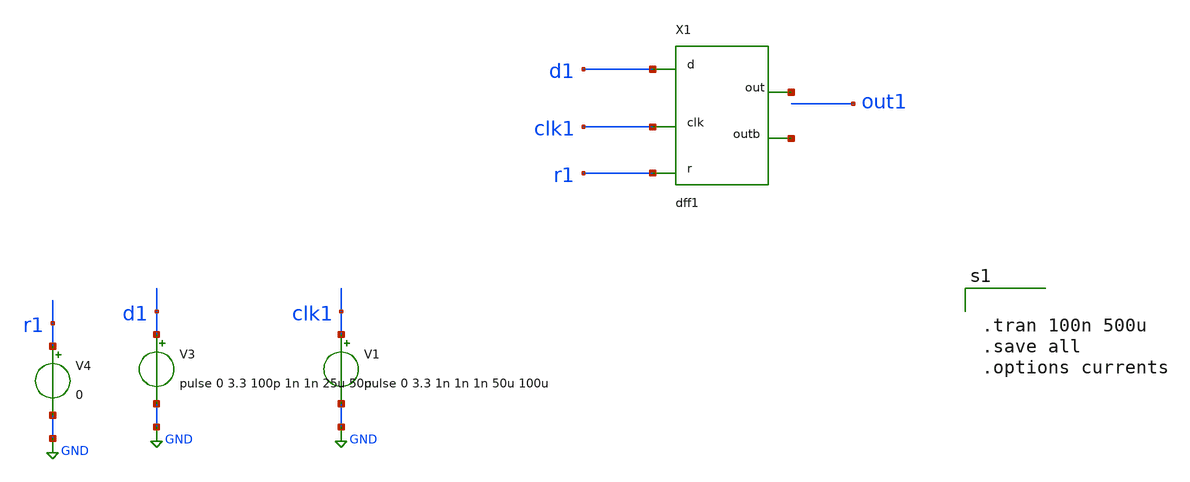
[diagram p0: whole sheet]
** sch_path: xschem/FDC/dff_sym_check.sch
**.subckt dff_sym_check
V1 clk1 GND pulse 0 3.3 1n 1n 1n 50u 100u
V3 d1 GND pulse 0 3.3 100p 1n 1n 25u 50u
V4 r1 GND 0
X1 clk1 d1 r1 net1 net2 dff1
**** begin user architecture code
  .lib /home/vinodhini/open_pdks/sky130/sky130A/libs.tech/ngspice/sky130.lib.spice tt


.tran 100n 500u
.save all
.options currents

**** end user architecture code
**.ends

* expanding   symbol:  /home/vinodhini/Documents/dff1.sym # of pins=5
** sym_path: xschem/FDC/dff1.sym
** sch_path: xschem/FDC/dff1.sch
.subckt dff1 clk d r q qbar
*.ipin clk
*.ipin d
*.ipin r
*.opin q
*.opin qbar
XM1 net2 clkbar net1 net1 sky130_fd_pr__nfet_g5v0d10v5 L=0.5 W=1 nf=1 ad='int((nf+1)/2) * W/nf * 0.29'
+ as='int((nf+2)/2) * W/nf * 0.29' pd='2*int((nf+1)/2) * (W/nf + 0.29)' ps='2*int((nf+2)/2) * (W/nf + 0.29)'
+ nrd='0.29 / W' nrs='0.29 / W' sa=0 sb=0 sd=0 mult=1 m=1
XM2 net2 dbar vdd vdd sky130_fd_pr__pfet_g5v0d10v5 L=0.5 W=2 nf=1 ad='int((nf+1)/2) * W/nf * 0.29' as='int((nf+2)/2) * W/nf * 0.29'
+ pd='2*int((nf+1)/2) * (W/nf + 0.29)' ps='2*int((nf+2)/2) * (W/nf + 0.29)' nrd='0.29 / W' nrs='0.29 / W'
+ sa=0 sb=0 sd=0 mult=1 m=1
XM3 out2 net2 vdd vdd sky130_fd_pr__pfet_g5v0d10v5 L=0.5 W=2 nf=1 ad='int((nf+1)/2) * W/nf * 0.29' as='int((nf+2)/2) * W/nf * 0.29'
+ pd='2*int((nf+1)/2) * (W/nf + 0.29)' ps='2*int((nf+2)/2) * (W/nf + 0.29)' nrd='0.29 / W' nrs='0.29 / W'
+ sa=0 sb=0 sd=0 mult=1 m=1
XM4 net1 dbar GND GND sky130_fd_pr__nfet_g5v0d10v5 L=0.5 W=1 nf=1 ad='int((nf+1)/2) * W/nf * 0.29' as='int((nf+2)/2) * W/nf * 0.29'
+ pd='2*int((nf+1)/2) * (W/nf + 0.29)' ps='2*int((nf+2)/2) * (W/nf + 0.29)' nrd='0.29 / W' nrs='0.29 / W'
+ sa=0 sb=0 sd=0 mult=1 m=1
XM5 out2 net2 GND GND sky130_fd_pr__nfet_g5v0d10v5 L=0.5 W=1 nf=1 ad='int((nf+1)/2) * W/nf * 0.29' as='int((nf+2)/2) * W/nf * 0.29'
+ pd='2*int((nf+1)/2) * (W/nf + 0.29)' ps='2*int((nf+2)/2) * (W/nf + 0.29)' nrd='0.29 / W' nrs='0.29 / W'
+ sa=0 sb=0 sd=0 mult=1 m=1
XM6 net2 clkbar vdd vdd sky130_fd_pr__pfet_g5v0d10v5 L=0.5 W=2 nf=1 ad='int((nf+1)/2) * W/nf * 0.29'
+ as='int((nf+2)/2) * W/nf * 0.29' pd='2*int((nf+1)/2) * (W/nf + 0.29)' ps='2*int((nf+2)/2) * (W/nf + 0.29)'
+ nrd='0.29 / W' nrs='0.29 / W' sa=0 sb=0 sd=0 mult=1 m=1
XM7 net4 d net3 net3 sky130_fd_pr__nfet_g5v0d10v5 L=0.5 W=1 nf=1 ad='int((nf+1)/2) * W/nf * 0.29' as='int((nf+2)/2) * W/nf * 0.29'
+ pd='2*int((nf+1)/2) * (W/nf + 0.29)' ps='2*int((nf+2)/2) * (W/nf + 0.29)' nrd='0.29 / W' nrs='0.29 / W'
+ sa=0 sb=0 sd=0 mult=1 m=1
XM8 net4 clkbar vdd vdd sky130_fd_pr__pfet_g5v0d10v5 L=0.5 W=2 nf=1 ad='int((nf+1)/2) * W/nf * 0.29'
+ as='int((nf+2)/2) * W/nf * 0.29' pd='2*int((nf+1)/2) * (W/nf + 0.29)' ps='2*int((nf+2)/2) * (W/nf + 0.29)'
+ nrd='0.29 / W' nrs='0.29 / W' sa=0 sb=0 sd=0 mult=1 m=1
XM9 out1 net4 vdd vdd sky130_fd_pr__pfet_g5v0d10v5 L=0.5 W=2 nf=1 ad='int((nf+1)/2) * W/nf * 0.29' as='int((nf+2)/2) * W/nf * 0.29'
+ pd='2*int((nf+1)/2) * (W/nf + 0.29)' ps='2*int((nf+2)/2) * (W/nf + 0.29)' nrd='0.29 / W' nrs='0.29 / W'
+ sa=0 sb=0 sd=0 mult=1 m=1
XM10 net3 clkbar GND GND sky130_fd_pr__nfet_g5v0d10v5 L=0.5 W=1 nf=1 ad='int((nf+1)/2) * W/nf * 0.29'
+ as='int((nf+2)/2) * W/nf * 0.29' pd='2*int((nf+1)/2) * (W/nf + 0.29)' ps='2*int((nf+2)/2) * (W/nf + 0.29)'
+ nrd='0.29 / W' nrs='0.29 / W' sa=0 sb=0 sd=0 mult=1 m=1
XM11 out1 net4 GND GND sky130_fd_pr__nfet_g5v0d10v5 L=0.5 W=1 nf=1 ad='int((nf+1)/2) * W/nf * 0.29' as='int((nf+2)/2) * W/nf * 0.29'
+ pd='2*int((nf+1)/2) * (W/nf + 0.29)' ps='2*int((nf+2)/2) * (W/nf + 0.29)' nrd='0.29 / W' nrs='0.29 / W'
+ sa=0 sb=0 sd=0 mult=1 m=1
XM12 net4 d vdd vdd sky130_fd_pr__pfet_g5v0d10v5 L=0.5 W=2 nf=1 ad='int((nf+1)/2) * W/nf * 0.29' as='int((nf+2)/2) * W/nf * 0.29'
+ pd='2*int((nf+1)/2) * (W/nf + 0.29)' ps='2*int((nf+2)/2) * (W/nf + 0.29)' nrd='0.29 / W' nrs='0.29 / W'
+ sa=0 sb=0 sd=0 mult=1 m=1
XM13 out3 out1 GND GND sky130_fd_pr__nfet_g5v0d10v5 L=0.5 W=1 nf=1 ad='int((nf+1)/2) * W/nf * 0.29' as='int((nf+2)/2) * W/nf * 0.29'
+ pd='2*int((nf+1)/2) * (W/nf + 0.29)' ps='2*int((nf+2)/2) * (W/nf + 0.29)' nrd='0.29 / W' nrs='0.29 / W'
+ sa=0 sb=0 sd=0 mult=1 m=1
XM15 out3 out4 GND GND sky130_fd_pr__nfet_g5v0d10v5 L=0.5 W=1 nf=1 ad='int((nf+1)/2) * W/nf * 0.29' as='int((nf+2)/2) * W/nf * 0.29'
+ pd='2*int((nf+1)/2) * (W/nf + 0.29)' ps='2*int((nf+2)/2) * (W/nf + 0.29)' nrd='0.29 / W' nrs='0.29 / W'
+ sa=0 sb=0 sd=0 mult=1 m=1
XM16 net5 out1 vdd vdd sky130_fd_pr__pfet_g5v0d10v5 L=0.5 W=2 nf=1 ad='int((nf+1)/2) * W/nf * 0.29' as='int((nf+2)/2) * W/nf * 0.29'
+ pd='2*int((nf+1)/2) * (W/nf + 0.29)' ps='2*int((nf+2)/2) * (W/nf + 0.29)' nrd='0.29 / W' nrs='0.29 / W'
+ sa=0 sb=0 sd=0 mult=1 m=1
XM14 out3 out4 net5 net5 sky130_fd_pr__pfet_g5v0d10v5 L=0.5 W=2 nf=1 ad='int((nf+1)/2) * W/nf * 0.29'
+ as='int((nf+2)/2) * W/nf * 0.29' pd='2*int((nf+1)/2) * (W/nf + 0.29)' ps='2*int((nf+2)/2) * (W/nf + 0.29)'
+ nrd='0.29 / W' nrs='0.29 / W' sa=0 sb=0 sd=0 mult=1 m=1
XM17 out4 out3 GND GND sky130_fd_pr__nfet_g5v0d10v5 L=0.5 W=1 nf=1 ad='int((nf+1)/2) * W/nf * 0.29' as='int((nf+2)/2) * W/nf * 0.29'
+ pd='2*int((nf+1)/2) * (W/nf + 0.29)' ps='2*int((nf+2)/2) * (W/nf + 0.29)' nrd='0.29 / W' nrs='0.29 / W'
+ sa=0 sb=0 sd=0 mult=1 m=1
XM18 out4 out2 GND GND sky130_fd_pr__nfet_g5v0d10v5 L=0.5 W=1 nf=1 ad='int((nf+1)/2) * W/nf * 0.29' as='int((nf+2)/2) * W/nf * 0.29'
+ pd='2*int((nf+1)/2) * (W/nf + 0.29)' ps='2*int((nf+2)/2) * (W/nf + 0.29)' nrd='0.29 / W' nrs='0.29 / W'
+ sa=0 sb=0 sd=0 mult=1 m=1
XM19 net6 out3 vdd vdd sky130_fd_pr__pfet_g5v0d10v5 L=0.5 W=2 nf=1 ad='int((nf+1)/2) * W/nf * 0.29' as='int((nf+2)/2) * W/nf * 0.29'
+ pd='2*int((nf+1)/2) * (W/nf + 0.29)' ps='2*int((nf+2)/2) * (W/nf + 0.29)' nrd='0.29 / W' nrs='0.29 / W'
+ sa=0 sb=0 sd=0 mult=1 m=1
XM20 out4 out2 net6 net6 sky130_fd_pr__pfet_g5v0d10v5 L=0.5 W=2 nf=1 ad='int((nf+1)/2) * W/nf * 0.29'
+ as='int((nf+2)/2) * W/nf * 0.29' pd='2*int((nf+1)/2) * (W/nf + 0.29)' ps='2*int((nf+2)/2) * (W/nf + 0.29)'
+ nrd='0.29 / W' nrs='0.29 / W' sa=0 sb=0 sd=0 mult=1 m=1
XM21 net8 out3 net7 net7 sky130_fd_pr__nfet_g5v0d10v5 L=0.5 W=1 nf=1 ad='int((nf+1)/2) * W/nf * 0.29'
+ as='int((nf+2)/2) * W/nf * 0.29' pd='2*int((nf+1)/2) * (W/nf + 0.29)' ps='2*int((nf+2)/2) * (W/nf + 0.29)'
+ nrd='0.29 / W' nrs='0.29 / W' sa=0 sb=0 sd=0 mult=1 m=1
XM22 net8 clk vdd vdd sky130_fd_pr__pfet_g5v0d10v5 L=0.5 W=2 nf=1 ad='int((nf+1)/2) * W/nf * 0.29' as='int((nf+2)/2) * W/nf * 0.29'
+ pd='2*int((nf+1)/2) * (W/nf + 0.29)' ps='2*int((nf+2)/2) * (W/nf + 0.29)' nrd='0.29 / W' nrs='0.29 / W'
+ sa=0 sb=0 sd=0 mult=1 m=1
XM23 out5 net8 vdd vdd sky130_fd_pr__pfet_g5v0d10v5 L=0.5 W=2 nf=1 ad='int((nf+1)/2) * W/nf * 0.29' as='int((nf+2)/2) * W/nf * 0.29'
+ pd='2*int((nf+1)/2) * (W/nf + 0.29)' ps='2*int((nf+2)/2) * (W/nf + 0.29)' nrd='0.29 / W' nrs='0.29 / W'
+ sa=0 sb=0 sd=0 mult=1 m=1
XM24 net7 clk GND GND sky130_fd_pr__nfet_g5v0d10v5 L=0.5 W=1 nf=1 ad='int((nf+1)/2) * W/nf * 0.29' as='int((nf+2)/2) * W/nf * 0.29'
+ pd='2*int((nf+1)/2) * (W/nf + 0.29)' ps='2*int((nf+2)/2) * (W/nf + 0.29)' nrd='0.29 / W' nrs='0.29 / W'
+ sa=0 sb=0 sd=0 mult=1 m=1
XM25 out5 net8 GND GND sky130_fd_pr__nfet_g5v0d10v5 L=0.5 W=1 nf=1 ad='int((nf+1)/2) * W/nf * 0.29' as='int((nf+2)/2) * W/nf * 0.29'
+ pd='2*int((nf+1)/2) * (W/nf + 0.29)' ps='2*int((nf+2)/2) * (W/nf + 0.29)' nrd='0.29 / W' nrs='0.29 / W'
+ sa=0 sb=0 sd=0 mult=1 m=1
XM26 net8 out3 vdd vdd sky130_fd_pr__pfet_g5v0d10v5 L=0.5 W=2 nf=1 ad='int((nf+1)/2) * W/nf * 0.29' as='int((nf+2)/2) * W/nf * 0.29'
+ pd='2*int((nf+1)/2) * (W/nf + 0.29)' ps='2*int((nf+2)/2) * (W/nf + 0.29)' nrd='0.29 / W' nrs='0.29 / W'
+ sa=0 sb=0 sd=0 mult=1 m=1
XM27 net10 clk net9 net9 sky130_fd_pr__nfet_g5v0d10v5 L=0.5 W=1 nf=1 ad='int((nf+1)/2) * W/nf * 0.29'
+ as='int((nf+2)/2) * W/nf * 0.29' pd='2*int((nf+1)/2) * (W/nf + 0.29)' ps='2*int((nf+2)/2) * (W/nf + 0.29)'
+ nrd='0.29 / W' nrs='0.29 / W' sa=0 sb=0 sd=0 mult=1 m=1
XM28 net10 out4 vdd vdd sky130_fd_pr__pfet_g5v0d10v5 L=0.5 W=2 nf=1 ad='int((nf+1)/2) * W/nf * 0.29'
+ as='int((nf+2)/2) * W/nf * 0.29' pd='2*int((nf+1)/2) * (W/nf + 0.29)' ps='2*int((nf+2)/2) * (W/nf + 0.29)'
+ nrd='0.29 / W' nrs='0.29 / W' sa=0 sb=0 sd=0 mult=1 m=1
XM29 out6 net10 vdd vdd sky130_fd_pr__pfet_g5v0d10v5 L=0.5 W=2 nf=1 ad='int((nf+1)/2) * W/nf * 0.29'
+ as='int((nf+2)/2) * W/nf * 0.29' pd='2*int((nf+1)/2) * (W/nf + 0.29)' ps='2*int((nf+2)/2) * (W/nf + 0.29)'
+ nrd='0.29 / W' nrs='0.29 / W' sa=0 sb=0 sd=0 mult=1 m=1
XM30 net9 out4 GND GND sky130_fd_pr__nfet_g5v0d10v5 L=0.5 W=1 nf=1 ad='int((nf+1)/2) * W/nf * 0.29' as='int((nf+2)/2) * W/nf * 0.29'
+ pd='2*int((nf+1)/2) * (W/nf + 0.29)' ps='2*int((nf+2)/2) * (W/nf + 0.29)' nrd='0.29 / W' nrs='0.29 / W'
+ sa=0 sb=0 sd=0 mult=1 m=1
XM31 out6 net10 GND GND sky130_fd_pr__nfet_g5v0d10v5 L=0.5 W=1 nf=1 ad='int((nf+1)/2) * W/nf * 0.29'
+ as='int((nf+2)/2) * W/nf * 0.29' pd='2*int((nf+1)/2) * (W/nf + 0.29)' ps='2*int((nf+2)/2) * (W/nf + 0.29)'
+ nrd='0.29 / W' nrs='0.29 / W' sa=0 sb=0 sd=0 mult=1 m=1
XM32 net10 clk vdd vdd sky130_fd_pr__pfet_g5v0d10v5 L=0.5 W=2 nf=1 ad='int((nf+1)/2) * W/nf * 0.29' as='int((nf+2)/2) * W/nf * 0.29'
+ pd='2*int((nf+1)/2) * (W/nf + 0.29)' ps='2*int((nf+2)/2) * (W/nf + 0.29)' nrd='0.29 / W' nrs='0.29 / W'
+ sa=0 sb=0 sd=0 mult=1 m=1
XM33 net12 r GND GND sky130_fd_pr__nfet_g5v0d10v5 L=0.5 W=1 nf=1 ad='int((nf+1)/2) * W/nf * 0.29' as='int((nf+2)/2) * W/nf * 0.29'
+ pd='2*int((nf+1)/2) * (W/nf + 0.29)' ps='2*int((nf+2)/2) * (W/nf + 0.29)' nrd='0.29 / W' nrs='0.29 / W'
+ sa=0 sb=0 sd=0 mult=1 m=1
XM34 net12 out5 GND GND sky130_fd_pr__nfet_g5v0d10v5 L=0.5 W=1 nf=1 ad='int((nf+1)/2) * W/nf * 0.29'
+ as='int((nf+2)/2) * W/nf * 0.29' pd='2*int((nf+1)/2) * (W/nf + 0.29)' ps='2*int((nf+2)/2) * (W/nf + 0.29)'
+ nrd='0.29 / W' nrs='0.29 / W' sa=0 sb=0 sd=0 mult=1 m=1
XM35 net11 r vdd vdd sky130_fd_pr__pfet_g5v0d10v5 L=0.5 W=2 nf=1 ad='int((nf+1)/2) * W/nf * 0.29' as='int((nf+2)/2) * W/nf * 0.29'
+ pd='2*int((nf+1)/2) * (W/nf + 0.29)' ps='2*int((nf+2)/2) * (W/nf + 0.29)' nrd='0.29 / W' nrs='0.29 / W'
+ sa=0 sb=0 sd=0 mult=1 m=1
XM36 net12 out5 net11 net11 sky130_fd_pr__pfet_g5v0d10v5 L=0.5 W=2 nf=1 ad='int((nf+1)/2) * W/nf * 0.29'
+ as='int((nf+2)/2) * W/nf * 0.29' pd='2*int((nf+1)/2) * (W/nf + 0.29)' ps='2*int((nf+2)/2) * (W/nf + 0.29)'
+ nrd='0.29 / W' nrs='0.29 / W' sa=0 sb=0 sd=0 mult=1 m=1
XM37 out7 net12 vdd vdd sky130_fd_pr__pfet_g5v0d10v5 L=0.5 W=2 nf=1 ad='int((nf+1)/2) * W/nf * 0.29'
+ as='int((nf+2)/2) * W/nf * 0.29' pd='2*int((nf+1)/2) * (W/nf + 0.29)' ps='2*int((nf+2)/2) * (W/nf + 0.29)'
+ nrd='0.29 / W' nrs='0.29 / W' sa=0 sb=0 sd=0 mult=1 m=1
XM38 out7 net12 GND GND sky130_fd_pr__nfet_g5v0d10v5 L=0.5 W=1 nf=1 ad='int((nf+1)/2) * W/nf * 0.29'
+ as='int((nf+2)/2) * W/nf * 0.29' pd='2*int((nf+1)/2) * (W/nf + 0.29)' ps='2*int((nf+2)/2) * (W/nf + 0.29)'
+ nrd='0.29 / W' nrs='0.29 / W' sa=0 sb=0 sd=0 mult=1 m=1
XM39 q out7 GND GND sky130_fd_pr__nfet_g5v0d10v5 L=0.5 W=1 nf=1 ad='int((nf+1)/2) * W/nf * 0.29' as='int((nf+2)/2) * W/nf * 0.29'
+ pd='2*int((nf+1)/2) * (W/nf + 0.29)' ps='2*int((nf+2)/2) * (W/nf + 0.29)' nrd='0.29 / W' nrs='0.29 / W'
+ sa=0 sb=0 sd=0 mult=1 m=1
XM40 q qbar GND GND sky130_fd_pr__nfet_g5v0d10v5 L=0.5 W=1 nf=1 ad='int((nf+1)/2) * W/nf * 0.29' as='int((nf+2)/2) * W/nf * 0.29'
+ pd='2*int((nf+1)/2) * (W/nf + 0.29)' ps='2*int((nf+2)/2) * (W/nf + 0.29)' nrd='0.29 / W' nrs='0.29 / W'
+ sa=0 sb=0 sd=0 mult=1 m=1
XM41 net13 out7 vdd vdd sky130_fd_pr__pfet_g5v0d10v5 L=0.5 W=2 nf=1 ad='int((nf+1)/2) * W/nf * 0.29'
+ as='int((nf+2)/2) * W/nf * 0.29' pd='2*int((nf+1)/2) * (W/nf + 0.29)' ps='2*int((nf+2)/2) * (W/nf + 0.29)'
+ nrd='0.29 / W' nrs='0.29 / W' sa=0 sb=0 sd=0 mult=1 m=1
XM42 q qbar net13 net13 sky130_fd_pr__pfet_g5v0d10v5 L=0.5 W=2 nf=1 ad='int((nf+1)/2) * W/nf * 0.29'
+ as='int((nf+2)/2) * W/nf * 0.29' pd='2*int((nf+1)/2) * (W/nf + 0.29)' ps='2*int((nf+2)/2) * (W/nf + 0.29)'
+ nrd='0.29 / W' nrs='0.29 / W' sa=0 sb=0 sd=0 mult=1 m=1
XM43 qbar q GND GND sky130_fd_pr__nfet_g5v0d10v5 L=0.5 W=1 nf=1 ad='int((nf+1)/2) * W/nf * 0.29' as='int((nf+2)/2) * W/nf * 0.29'
+ pd='2*int((nf+1)/2) * (W/nf + 0.29)' ps='2*int((nf+2)/2) * (W/nf + 0.29)' nrd='0.29 / W' nrs='0.29 / W'
+ sa=0 sb=0 sd=0 mult=1 m=1
XM44 qbar out6 GND GND sky130_fd_pr__nfet_g5v0d10v5 L=0.5 W=1 nf=1 ad='int((nf+1)/2) * W/nf * 0.29' as='int((nf+2)/2) * W/nf * 0.29'
+ pd='2*int((nf+1)/2) * (W/nf + 0.29)' ps='2*int((nf+2)/2) * (W/nf + 0.29)' nrd='0.29 / W' nrs='0.29 / W'
+ sa=0 sb=0 sd=0 mult=1 m=1
XM45 net14 q vdd vdd sky130_fd_pr__pfet_g5v0d10v5 L=0.5 W=2 nf=1 ad='int((nf+1)/2) * W/nf * 0.29' as='int((nf+2)/2) * W/nf * 0.29'
+ pd='2*int((nf+1)/2) * (W/nf + 0.29)' ps='2*int((nf+2)/2) * (W/nf + 0.29)' nrd='0.29 / W' nrs='0.29 / W'
+ sa=0 sb=0 sd=0 mult=1 m=1
XM46 qbar out6 net14 net14 sky130_fd_pr__pfet_g5v0d10v5 L=0.5 W=2 nf=1 ad='int((nf+1)/2) * W/nf * 0.29'
+ as='int((nf+2)/2) * W/nf * 0.29' pd='2*int((nf+1)/2) * (W/nf + 0.29)' ps='2*int((nf+2)/2) * (W/nf + 0.29)'
+ nrd='0.29 / W' nrs='0.29 / W' sa=0 sb=0 sd=0 mult=1 m=1
XM47 clkbar clk vdd vdd sky130_fd_pr__pfet_g5v0d10v5 L=0.5 W=2 nf=1 ad='int((nf+1)/2) * W/nf * 0.29'
+ as='int((nf+2)/2) * W/nf * 0.29' pd='2*int((nf+1)/2) * (W/nf + 0.29)' ps='2*int((nf+2)/2) * (W/nf + 0.29)'
+ nrd='0.29 / W' nrs='0.29 / W' sa=0 sb=0 sd=0 mult=1 m=1
XM48 clkbar clk GND GND sky130_fd_pr__nfet_g5v0d10v5 L=0.5 W=1 nf=1 ad='int((nf+1)/2) * W/nf * 0.29'
+ as='int((nf+2)/2) * W/nf * 0.29' pd='2*int((nf+1)/2) * (W/nf + 0.29)' ps='2*int((nf+2)/2) * (W/nf + 0.29)'
+ nrd='0.29 / W' nrs='0.29 / W' sa=0 sb=0 sd=0 mult=1 m=1
XM49 dbar d vdd vdd sky130_fd_pr__pfet_g5v0d10v5 L=0.5 W=2 nf=1 ad='int((nf+1)/2) * W/nf * 0.29' as='int((nf+2)/2) * W/nf * 0.29'
+ pd='2*int((nf+1)/2) * (W/nf + 0.29)' ps='2*int((nf+2)/2) * (W/nf + 0.29)' nrd='0.29 / W' nrs='0.29 / W'
+ sa=0 sb=0 sd=0 mult=1 m=1
XM50 dbar d GND GND sky130_fd_pr__nfet_g5v0d10v5 L=0.5 W=1 nf=1 ad='int((nf+1)/2) * W/nf * 0.29' as='int((nf+2)/2) * W/nf * 0.29'
+ pd='2*int((nf+1)/2) * (W/nf + 0.29)' ps='2*int((nf+2)/2) * (W/nf + 0.29)' nrd='0.29 / W' nrs='0.29 / W'
+ sa=0 sb=0 sd=0 mult=1 m=1
V3 vdd GND 3.3
.ends

.GLOBAL GND
.end
